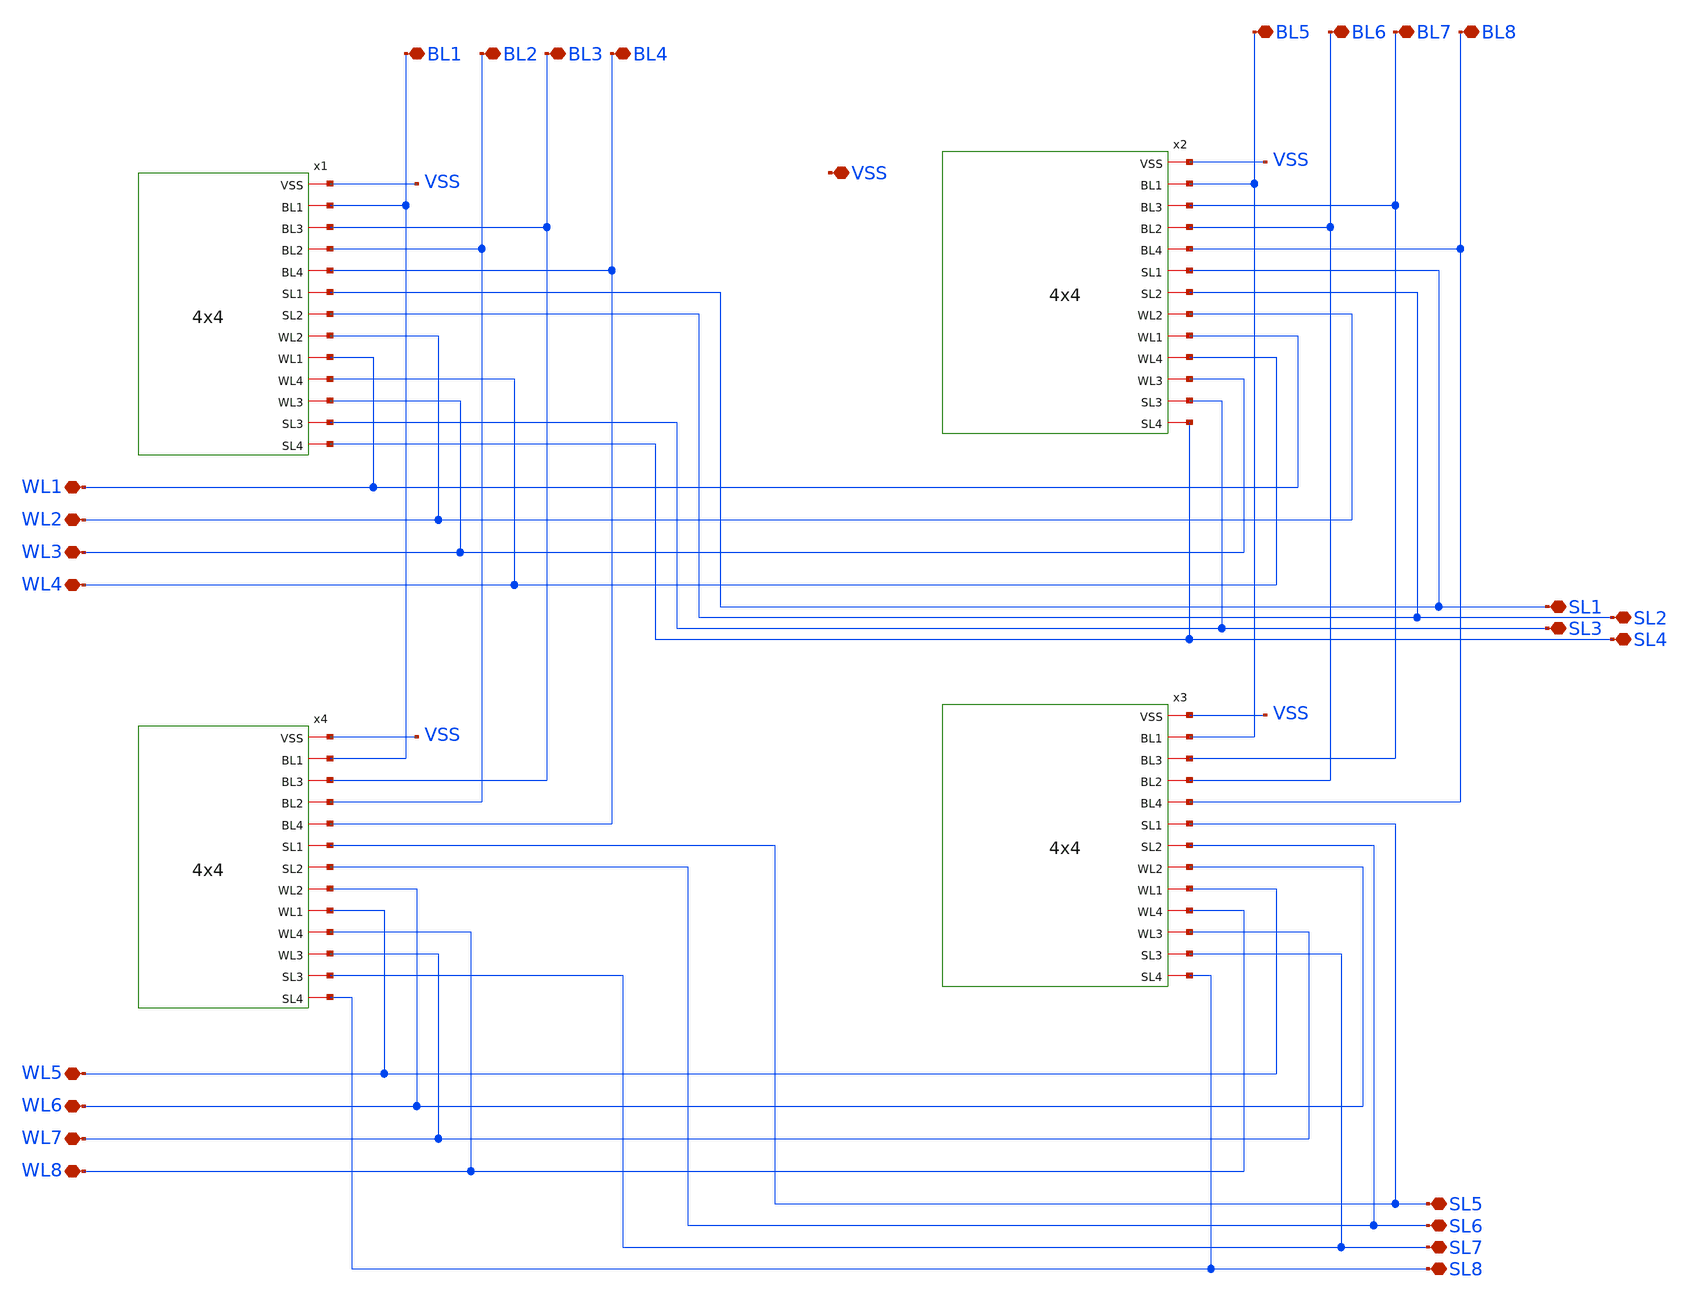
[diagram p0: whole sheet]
** sch_path: xschem/Crossbar/8x8.sch
* StefanSchippers/xschem_sky130/sky130_fd_pr/reram.sym:
* Copyright 2021 Stefan Frederik Schippers
* Licensed under the Apache License, Version 2.0 (the "License");
**.subckt 8x8 BL1 BL2 BL3 BL4 BL5 BL6 BL7 BL8 SL1 WL1 WL2 WL3 WL4 WL5 WL6 WL7 WL8 SL2 SL3 SL4 SL5
*+ SL6 SL7 SL8 VSS
*.iopin BL1
*.iopin BL2
*.iopin BL3
*.iopin BL4
*.iopin BL5
*.iopin BL6
*.iopin BL7
*.iopin BL8
*.iopin SL1
*.iopin WL1
*.iopin WL2
*.iopin WL3
*.iopin WL4
*.iopin WL5
*.iopin WL6
*.iopin WL7
*.iopin WL8
*.iopin SL2
*.iopin SL3
*.iopin SL4
*.iopin SL5
*.iopin SL6
*.iopin SL7
*.iopin SL8
*.iopin VSS
x1 VSS BL1 BL3 BL2 BL4 SL1 SL2 WL2 WL1 WL4 WL3 SL3 SL4 4x4
x2 VSS BL5 BL7 BL6 BL8 SL1 SL2 WL2 WL1 WL4 WL3 SL3 SL4 4x4
x3 VSS BL5 BL7 BL6 BL8 SL5 SL6 WL6 WL5 WL8 WL7 SL7 SL8 4x4
x4 VSS BL1 BL3 BL2 BL4 SL5 SL6 WL6 WL5 WL8 WL7 SL7 SL8 4x4
**.ends

* expanding   symbol:  Crossbar/4x4.sym # of pins=13
** sym_path: xschem/4x4.sym
** sch_path: xschem/4x4.sch
.subckt 4x4 VSS BL1 BL3 BL2 BL4 SL1 SL2 WL2 WL1 WL4 WL3 SL3 SL4
*.iopin BL1
*.iopin BL2
*.iopin SL2
*.iopin SL1
*.iopin BL3
*.iopin BL4
*.iopin SL4
*.iopin SL3
*.iopin WL2
*.iopin WL1
*.iopin WL4
*.iopin WL3
*.iopin VSS
x1 VSS BL2 BL1 WL1 SL1 WL2 SL2 2x2
x2 VSS BL2 BL1 WL3 SL3 WL4 SL4 2x2
x3 VSS BL4 BL3 WL1 SL1 WL2 SL2 2x2
x4 VSS BL4 BL3 WL3 SL3 WL4 SL4 2x2
.ends


* expanding   symbol:  2x2.sym # of pins=7
** sym_path: xschem/Crossbar/2x2.sym
** sch_path: xschem/Crossbar/2x2.sch
.subckt 2x2 VSS BL2 BL1 WL1 SL1 WL2 SL2
*.iopin BL2
*.iopin BL1
*.iopin VSS
*.iopin WL1
*.iopin WL2
*.iopin SL1
*.iopin SL2
x1 BL1 WL1 VSS SL1 1T1R
x2 BL2 WL1 VSS SL1 1T1R
x3 BL1 WL2 VSS SL2 1T1R
x4 BL2 WL2 VSS SL2 1T1R
.ends


* expanding   symbol:  Crossbar/1T1R.sym # of pins=4
** sym_path: xschem/1T1R.sym
** sch_path: xschem/1T1R.sch
.subckt 1T1R BL WL VSS SL
*.iopin SL
*.iopin VSS
*.iopin WL
*.iopin BL
XR1 BL net1 sky130_fd_pr_reram__reram_cell Tfilament_0=3.8e-9
XM1 net1 WL SL VSS sky130_fd_pr__nfet_g5v0d10v5 L=0.5 W=7 nf=1 ad='int((nf+1)/2) * W/nf * 0.29' as='int((nf+2)/2) * W/nf * 0.29'
+ pd='2*int((nf+1)/2) * (W/nf + 0.29)' ps='2*int((nf+2)/2) * (W/nf + 0.29)' nrd='0.29 / W' nrs='0.29 / W'
+ sa=0 sb=0 sd=0 mult=1 m=1
.ends

**** begin user architecture code

.subckt sky130_fd_pr_reram__reram_cell TE BE Tfilament_0=3.3e-9 area_ox=0.1024e-12
N1 TE BE nFilament sky130_fd_pr_reram__reram_model
.ic v(nFilament)={Tfilament_0*1.0e9}
.ends sky130_fd_pr_reram__reram_cell

.model sky130_fd_pr_reram__reram_model sky130_fd_pr_reram__reram_module  area_ox = 0.1024e-12  Tox =
+ 5.0  Tfilament_max = 4.9  Tfilament_min = 3.3  Eact_generation = 1.501  Eact_recombination  = 1.500
+  I_k1  = 6.140e-5  Tfilament_ref = 4.7249  V_ref = 0.430  velocity_k1 = 150  gamma_k0  = 16.5  gamma_k1
+  = -1.25  Temperature_0 = 300  C_thermal = 3.1825e-16  tau_thermal = 0.23e-9  t_step  = 1.0e-9
+  smoothing = 1e-7  Kclip = 200

.control
pre_osdi $SKYWATER_MODELS/sky130_fd_pr_reram__reram_module.osdi
.endc

**** end user architecture code
.end
